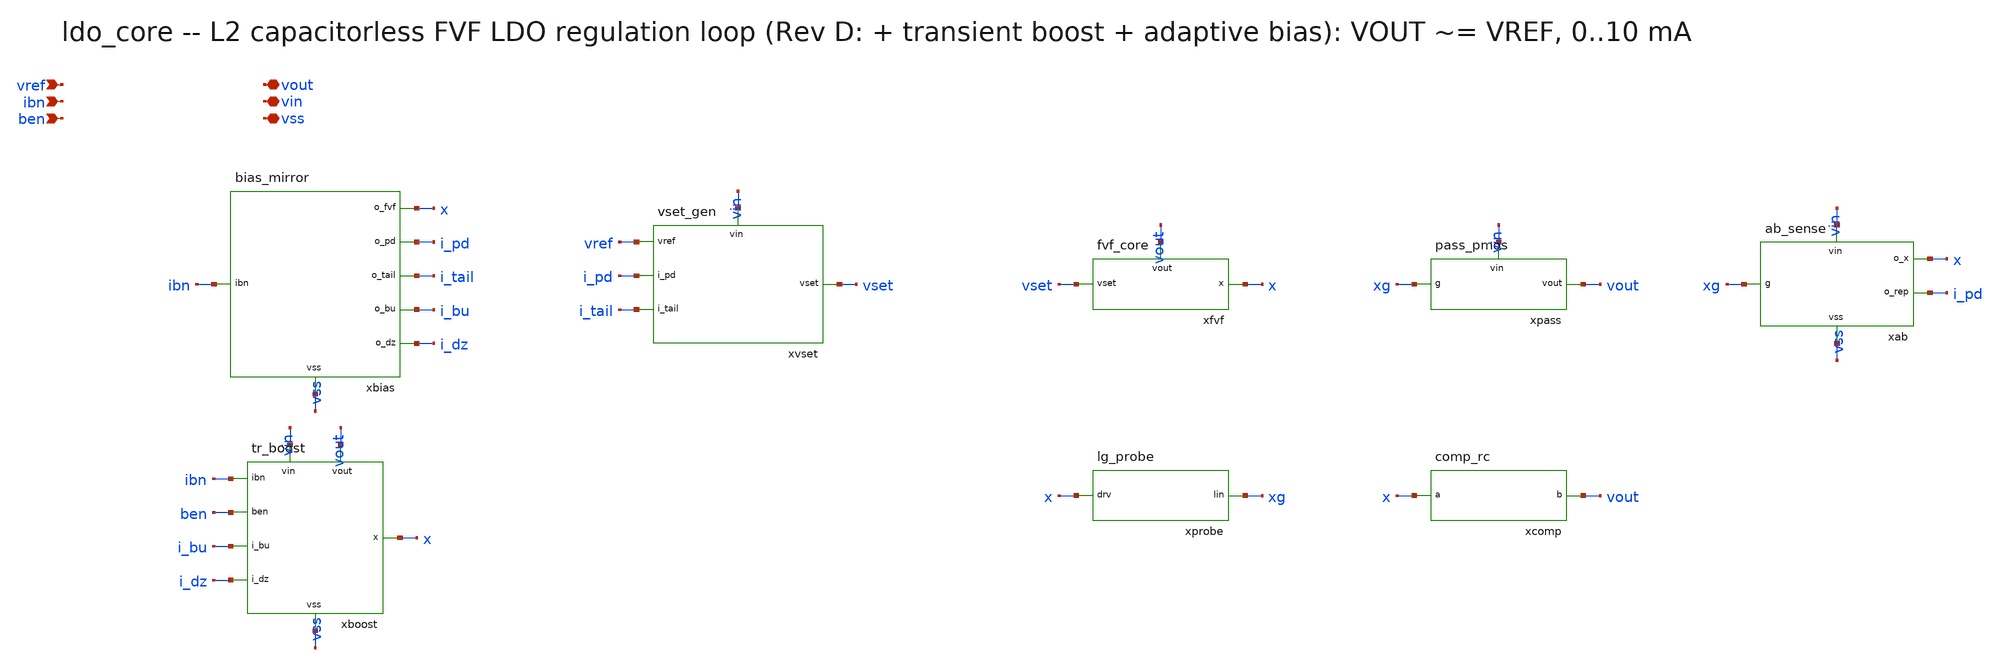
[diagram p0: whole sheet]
** sch_path: xschem/onetops/ldo_core.sch
**.subckt ldo_core vref ibn ben vout vin vss
*.ipin vref
*.ipin ibn
*.ipin ben
*.iopin vout
*.iopin vin
*.iopin vss
xbias ibn x i_pd i_tail i_bu i_dz vss bias_mirror
xboost ibn ben i_bu i_dz x vin vout vss tr_boost
xvset vref i_pd i_tail vset vin vset_gen
xfvf vset x vout fvf_core
xprobe x xg lg_probe
xpass xg vout vin pass_pmos
xcomp x vout comp_rc
xab xg x i_pd vin vss ab_sense
**.ends

* expanding   symbol:  onetops/bias_mirror.sym # of pins=7
** sym_path: xschem/onetops/bias_mirror.sym
** sch_path: xschem/onetops/bias_mirror.sch
.subckt bias_mirror ibn o_fvf o_pd o_tail o_bu o_dz vss
*.ipin ibn
*.opin o_fvf
*.opin o_pd
*.opin o_tail
*.opin o_bu
*.opin o_dz
*.iopin vss
XMN0 ibn ibn vss vss sky130_fd_pr__nfet_01v8 L=1 W=4 nf=1 ad='int((1 + 1)/2) * 4 / 1 * 0.29' as='int((1 + 2)/2) * 4 / 1 * 0.29'
+ pd='2*int((1 + 1)/2) * (4 / 1 + 0.29)' ps='2*int((1 + 2)/2) * (4 / 1 + 0.29)' nrd='0.29 / 4 ' nrs='0.29 / 4 '
+ sa=0 sb=0 sd=0 mult=1 m=1
XMN1 o_fvf ibn vss vss sky130_fd_pr__nfet_01v8 L=1 W=1 nf=1 ad='int((1 + 1)/2) * 1 / 1 * 0.29' as='int((1 + 2)/2) * 1 / 1 * 0.29'
+ pd='2*int((1 + 1)/2) * (1 / 1 + 0.29)' ps='2*int((1 + 2)/2) * (1 / 1 + 0.29)' nrd='0.29 / 1 ' nrs='0.29 / 1 '
+ sa=0 sb=0 sd=0 mult=1 m=1
XMN2 o_bu ibn vss vss sky130_fd_pr__nfet_01v8 L=1 W=4 nf=1 ad='int((1 + 1)/2) * 4 / 1 * 0.29' as='int((1 + 2)/2) * 4 / 1 * 0.29'
+ pd='2*int((1 + 1)/2) * (4 / 1 + 0.29)' ps='2*int((1 + 2)/2) * (4 / 1 + 0.29)' nrd='0.29 / 4 ' nrs='0.29 / 4 '
+ sa=0 sb=0 sd=0 mult=1 m=1
XMN3 o_pd ibn vss vss sky130_fd_pr__nfet_01v8 L=1 W=1 nf=1 ad='int((1 + 1)/2) * 1 / 1 * 0.29' as='int((1 + 2)/2) * 1 / 1 * 0.29'
+ pd='2*int((1 + 1)/2) * (1 / 1 + 0.29)' ps='2*int((1 + 2)/2) * (1 / 1 + 0.29)' nrd='0.29 / 1 ' nrs='0.29 / 1 '
+ sa=0 sb=0 sd=0 mult=1 m=1
XMN4 o_tail ibn vss vss sky130_fd_pr__nfet_01v8 L=1 W=4 nf=1 ad='int((1 + 1)/2) * 4 / 1 * 0.29' as='int((1 + 2)/2) * 4 / 1 * 0.29'
+ pd='2*int((1 + 1)/2) * (4 / 1 + 0.29)' ps='2*int((1 + 2)/2) * (4 / 1 + 0.29)' nrd='0.29 / 4 ' nrs='0.29 / 4 '
+ sa=0 sb=0 sd=0 mult=2 m=2
XMN5 o_dz ibn vss vss sky130_fd_pr__nfet_01v8 L=1 W=4 nf=1 ad='int((1 + 1)/2) * 4 / 1 * 0.29' as='int((1 + 2)/2) * 4 / 1 * 0.29'
+ pd='2*int((1 + 1)/2) * (4 / 1 + 0.29)' ps='2*int((1 + 2)/2) * (4 / 1 + 0.29)' nrd='0.29 / 4 ' nrs='0.29 / 4 '
+ sa=0 sb=0 sd=0 mult=1 m=1
.ends


* expanding   symbol:  onetops/tr_boost.sym # of pins=8
** sym_path: xschem/onetops/tr_boost.sym
** sch_path: xschem/onetops/tr_boost.sch
.subckt tr_boost ibn ben i_bu i_dz x vin vout vss
*.ipin ibn
*.ipin ben
*.iopin i_bu
*.iopin i_dz
*.iopin x
*.iopin vin
*.iopin vout
*.iopin vss
XMPB0 i_bu i_bu vin vin sky130_fd_pr__pfet_01v8_lvt L=0.5 W=40 nf=1 ad='int((1 + 1)/2) * 40 / 1 * 0.29'
+ as='int((1 + 2)/2) * 40 / 1 * 0.29' pd='2*int((1 + 1)/2) * (40 / 1 + 0.29)' ps='2*int((1 + 2)/2) * (40 / 1 + 0.29)'
+ nrd='0.29 / 40 ' nrs='0.29 / 40 ' sa=0 sb=0 sd=0 mult=1 m=1
Rbu i_bu gsu 1Meg m=1
Cbu vout gsu 0.5p m=1
XMPB1 i_dz gsu vin vin sky130_fd_pr__pfet_01v8_lvt L=0.5 W=20 nf=1 ad='int((1 + 1)/2) * 20 / 1 * 0.29'
+ as='int((1 + 2)/2) * 20 / 1 * 0.29' pd='2*int((1 + 1)/2) * (20 / 1 + 0.29)' ps='2*int((1 + 2)/2) * (20 / 1 + 0.29)'
+ nrd='0.29 / 20 ' nrs='0.29 / 20 ' sa=0 sb=0 sd=0 mult=1 m=1
XMNB0 i_dz i_dz vss vss sky130_fd_pr__nfet_01v8 L=0.5 W=2 nf=1 ad='int((1 + 1)/2) * 2 / 1 * 0.29' as='int((1 + 2)/2) * 2 / 1 * 0.29'
+ pd='2*int((1 + 1)/2) * (2 / 1 + 0.29)' ps='2*int((1 + 2)/2) * (2 / 1 + 0.29)' nrd='0.29 / 2 ' nrs='0.29 / 2 '
+ sa=0 sb=0 sd=0 mult=1 m=1
XMNB1 nsw i_dz vss vss sky130_fd_pr__nfet_01v8 L=0.5 W=2 nf=1 ad='int((1 + 1)/2) * 2 / 1 * 0.29' as='int((1 + 2)/2) * 2 / 1 * 0.29'
+ pd='2*int((1 + 1)/2) * (2 / 1 + 0.29)' ps='2*int((1 + 2)/2) * (2 / 1 + 0.29)' nrd='0.29 / 2 ' nrs='0.29 / 2 '
+ sa=0 sb=0 sd=0 mult=20 m=20
XMSW x ben nsw vss sky130_fd_pr__nfet_01v8 L=0.15 W=10 nf=1 ad='int((1 + 1)/2) * 10 / 1 * 0.29' as='int((1 + 2)/2) * 10 / 1 * 0.29'
+ pd='2*int((1 + 1)/2) * (10 / 1 + 0.29)' ps='2*int((1 + 2)/2) * (10 / 1 + 0.29)' nrd='0.29 / 10 ' nrs='0.29 / 10 '
+ sa=0 sb=0 sd=0 mult=1 m=1
Rbo ibn gso 1Meg m=1
Cbo vout gso 0.5p m=1
XMND vout gso vss vss sky130_fd_pr__nfet_01v8 L=1 W=4 nf=1 ad='int((1 + 1)/2) * 4 / 1 * 0.29' as='int((1 + 2)/2) * 4 / 1 * 0.29'
+ pd='2*int((1 + 1)/2) * (4 / 1 + 0.29)' ps='2*int((1 + 2)/2) * (4 / 1 + 0.29)' nrd='0.29 / 4 ' nrs='0.29 / 4 '
+ sa=0 sb=0 sd=0 mult=2 m=2
XMPDZ ndo i_bu vin vin sky130_fd_pr__pfet_01v8_lvt L=0.5 W=40 nf=1 ad='int((1 + 1)/2) * 40 / 1 * 0.29'
+ as='int((1 + 2)/2) * 40 / 1 * 0.29' pd='2*int((1 + 1)/2) * (40 / 1 + 0.29)' ps='2*int((1 + 2)/2) * (40 / 1 + 0.29)'
+ nrd='0.29 / 40 ' nrs='0.29 / 40 ' sa=0 sb=0 sd=0 mult=1 m=1
XMNS1 ndo gso vss vss sky130_fd_pr__nfet_01v8 L=1 W=2 nf=1 ad='int((1 + 1)/2) * 2 / 1 * 0.29' as='int((1 + 2)/2) * 2 / 1 * 0.29'
+ pd='2*int((1 + 1)/2) * (2 / 1 + 0.29)' ps='2*int((1 + 2)/2) * (2 / 1 + 0.29)' nrd='0.29 / 2 ' nrs='0.29 / 2 '
+ sa=0 sb=0 sd=0 mult=1 m=1
XMPO0 ndo ndo vin vin sky130_fd_pr__pfet_01v8 L=0.5 W=4 nf=1 ad='int((1 + 1)/2) * 4 / 1 * 0.29' as='int((1 + 2)/2) * 4 / 1 * 0.29'
+ pd='2*int((1 + 1)/2) * (4 / 1 + 0.29)' ps='2*int((1 + 2)/2) * (4 / 1 + 0.29)' nrd='0.29 / 4 ' nrs='0.29 / 4 '
+ sa=0 sb=0 sd=0 mult=1 m=1
XMPO1 psw ndo vin vin sky130_fd_pr__pfet_01v8 L=0.5 W=4 nf=1 ad='int((1 + 1)/2) * 4 / 1 * 0.29' as='int((1 + 2)/2) * 4 / 1 * 0.29'
+ pd='2*int((1 + 1)/2) * (4 / 1 + 0.29)' ps='2*int((1 + 2)/2) * (4 / 1 + 0.29)' nrd='0.29 / 4 ' nrs='0.29 / 4 '
+ sa=0 sb=0 sd=0 mult=20 m=20
XMPSW x benb psw vin sky130_fd_pr__pfet_01v8 L=0.15 W=20 nf=1 ad='int((1 + 1)/2) * 20 / 1 * 0.29' as='int((1 + 2)/2) * 20 / 1 * 0.29'
+ pd='2*int((1 + 1)/2) * (20 / 1 + 0.29)' ps='2*int((1 + 2)/2) * (20 / 1 + 0.29)' nrd='0.29 / 20 ' nrs='0.29 / 20 '
+ sa=0 sb=0 sd=0 mult=1 m=1
xinv ben benb vin vss inv
.ends


* expanding   symbol:  onetops/vset_gen.sym # of pins=5
** sym_path: xschem/onetops/vset_gen.sym
** sch_path: xschem/onetops/vset_gen.sch
.subckt vset_gen vref i_pd i_tail vset vin
*.ipin vref
*.opin vset
*.iopin i_pd
*.iopin i_tail
*.iopin vin
XMPD i_pd i_pd vin vin sky130_fd_pr__pfet_01v8_lvt L=2 W=10 nf=1 ad='int((1 + 1)/2) * 10 / 1 * 0.29'
+ as='int((1 + 2)/2) * 10 / 1 * 0.29' pd='2*int((1 + 1)/2) * (10 / 1 + 0.29)' ps='2*int((1 + 2)/2) * (10 / 1 + 0.29)'
+ nrd='0.29 / 10 ' nrs='0.29 / 10 ' sa=0 sb=0 sd=0 mult=1 m=1
XMPS vrep i_pd vin vin sky130_fd_pr__pfet_01v8_lvt L=2 W=10 nf=1 ad='int((1 + 1)/2) * 10 / 1 * 0.29'
+ as='int((1 + 2)/2) * 10 / 1 * 0.29' pd='2*int((1 + 1)/2) * (10 / 1 + 0.29)' ps='2*int((1 + 2)/2) * (10 / 1 + 0.29)'
+ nrd='0.29 / 10 ' nrs='0.29 / 10 ' sa=0 sb=0 sd=0 mult=1 m=1
XMR 0 vset vrep vrep sky130_fd_pr__pfet_01v8_lvt L=1 W=100 nf=1 ad='int((1 + 1)/2) * 100 / 1 * 0.29'
+ as='int((1 + 2)/2) * 100 / 1 * 0.29' pd='2*int((1 + 1)/2) * (100 / 1 + 0.29)' ps='2*int((1 + 2)/2) * (100 / 1 + 0.29)'
+ nrd='0.29 / 100 ' nrs='0.29 / 100 ' sa=0 sb=0 sd=0 mult=1 m=1
xota vref vrep i_tail vset vin ota5t
Cset vset 0 2p m=1
.ends


* expanding   symbol:  onetops/fvf_core.sym # of pins=3
** sym_path: xschem/onetops/fvf_core.sym
** sch_path: xschem/onetops/fvf_core.sch
.subckt fvf_core vset x vout
*.ipin vset
*.opin x
*.iopin vout
XMC x vset vout vout sky130_fd_pr__pfet_01v8_lvt L=1 W=100 nf=1 ad='int((1 + 1)/2) * 100 / 1 * 0.29'
+ as='int((1 + 2)/2) * 100 / 1 * 0.29' pd='2*int((1 + 1)/2) * (100 / 1 + 0.29)' ps='2*int((1 + 2)/2) * (100 / 1 + 0.29)'
+ nrd='0.29 / 100 ' nrs='0.29 / 100 ' sa=0 sb=0 sd=0 mult=1 m=1
.ends


* expanding   symbol:  onetops/lg_probe.sym # of pins=2
** sym_path: xschem/onetops/lg_probe.sym
** sch_path: xschem/onetops/lg_probe.sch
.subckt lg_probe drv lin
*.iopin drv
*.iopin lin
Vbrk lin drv dc 0 ac 0
Iinj 0 lin dc 0 ac 0
.ends


* expanding   symbol:  onetops/pass_pmos.sym # of pins=3
** sym_path: xschem/onetops/pass_pmos.sym
** sch_path: xschem/onetops/pass_pmos.sch
.subckt pass_pmos g vout vin
*.ipin g
*.iopin vin
*.iopin vout
XMP vout g vin vin sky130_fd_pr__pfet_01v8 L=0.35 W=10 nf=1 ad='int((1 + 1)/2) * 10 / 1 * 0.29' as='int((1 + 2)/2) * 10 / 1 * 0.29'
+ pd='2*int((1 + 1)/2) * (10 / 1 + 0.29)' ps='2*int((1 + 2)/2) * (10 / 1 + 0.29)' nrd='0.29 / 10 ' nrs='0.29 / 10 '
+ sa=0 sb=0 sd=0 mult=70 m=70
.ends


* expanding   symbol:  onetops/comp_rc.sym # of pins=2
** sym_path: xschem/onetops/comp_rc.sym
** sch_path: xschem/onetops/comp_rc.sch
.subckt comp_rc a b
*.iopin a
*.iopin b
Rz a n1 1 m=1
Cc n1 b 4p m=1
.ends


* expanding   symbol:  onetops/ab_sense.sym # of pins=5
** sym_path: xschem/onetops/ab_sense.sym
** sch_path: xschem/onetops/ab_sense.sch
.subckt ab_sense g o_x o_rep vin vss
*.ipin g
*.opin o_x
*.opin o_rep
*.iopin vin
*.iopin vss
XMS ns g vin vin sky130_fd_pr__pfet_01v8 L=0.35 W=1.4 nf=1 ad='int((1 + 1)/2) * 1.4 / 1 * 0.29' as='int((1 + 2)/2) * 1.4 / 1 * 0.29'
+ pd='2*int((1 + 1)/2) * (1.4 / 1 + 0.29)' ps='2*int((1 + 2)/2) * (1.4 / 1 + 0.29)' nrd='0.29 / 1.4 ' nrs='0.29 / 1.4 '
+ sa=0 sb=0 sd=0 mult=1 m=1
XMSD ns ns vss vss sky130_fd_pr__nfet_01v8 L=1 W=4 nf=1 ad='int((1 + 1)/2) * 4 / 1 * 0.29' as='int((1 + 2)/2) * 4 / 1 * 0.29'
+ pd='2*int((1 + 1)/2) * (4 / 1 + 0.29)' ps='2*int((1 + 2)/2) * (4 / 1 + 0.29)' nrd='0.29 / 4 ' nrs='0.29 / 4 '
+ sa=0 sb=0 sd=0 mult=1 m=1
XMSX o_x ns vss vss sky130_fd_pr__nfet_01v8 L=1 W=4 nf=1 ad='int((1 + 1)/2) * 4 / 1 * 0.29' as='int((1 + 2)/2) * 4 / 1 * 0.29'
+ pd='2*int((1 + 1)/2) * (4 / 1 + 0.29)' ps='2*int((1 + 2)/2) * (4 / 1 + 0.29)' nrd='0.29 / 4 ' nrs='0.29 / 4 '
+ sa=0 sb=0 sd=0 mult=1 m=1
XMSR o_rep ns vss vss sky130_fd_pr__nfet_01v8 L=1 W=4 nf=1 ad='int((1 + 1)/2) * 4 / 1 * 0.29' as='int((1 + 2)/2) * 4 / 1 * 0.29'
+ pd='2*int((1 + 1)/2) * (4 / 1 + 0.29)' ps='2*int((1 + 2)/2) * (4 / 1 + 0.29)' nrd='0.29 / 4 ' nrs='0.29 / 4 '
+ sa=0 sb=0 sd=0 mult=1 m=1
.ends


* expanding   symbol:  onetops/inv.sym # of pins=4
** sym_path: xschem/onetops/inv.sym
** sch_path: xschem/onetops/inv.sch
.subckt inv a y vdd vss
*.ipin a
*.opin y
*.iopin vdd
*.iopin vss
XMP1 y a vdd vdd sky130_fd_pr__pfet_01v8 L=0.15 W=2 nf=1 ad='int((1 + 1)/2) * 2 / 1 * 0.29' as='int((1 + 2)/2) * 2 / 1 * 0.29'
+ pd='2*int((1 + 1)/2) * (2 / 1 + 0.29)' ps='2*int((1 + 2)/2) * (2 / 1 + 0.29)' nrd='0.29 / 2 ' nrs='0.29 / 2 '
+ sa=0 sb=0 sd=0 mult=1 m=1
XMN1 y a vss vss sky130_fd_pr__nfet_01v8 L=0.15 W=1 nf=1 ad='int((1 + 1)/2) * 1 / 1 * 0.29' as='int((1 + 2)/2) * 1 / 1 * 0.29'
+ pd='2*int((1 + 1)/2) * (1 / 1 + 0.29)' ps='2*int((1 + 2)/2) * (1 / 1 + 0.29)' nrd='0.29 / 1 ' nrs='0.29 / 1 '
+ sa=0 sb=0 sd=0 mult=1 m=1
.ends


* expanding   symbol:  onetops/ota5t.sym # of pins=5
** sym_path: xschem/onetops/ota5t.sym
** sch_path: xschem/onetops/ota5t.sch
.subckt ota5t inp inn tail out vdd
*.ipin inp
*.ipin inn
*.opin out
*.iopin tail
*.iopin vdd
XMP1 nd nd vdd vdd sky130_fd_pr__pfet_01v8_lvt L=2 W=20 nf=1 ad='int((1 + 1)/2) * 20 / 1 * 0.29' as='int((1 + 2)/2) * 20 / 1 * 0.29'
+ pd='2*int((1 + 1)/2) * (20 / 1 + 0.29)' ps='2*int((1 + 2)/2) * (20 / 1 + 0.29)' nrd='0.29 / 20 ' nrs='0.29 / 20 '
+ sa=0 sb=0 sd=0 mult=1 m=1
XMP2 out nd vdd vdd sky130_fd_pr__pfet_01v8_lvt L=2 W=20 nf=1 ad='int((1 + 1)/2) * 20 / 1 * 0.29' as='int((1 + 2)/2) * 20 / 1 * 0.29'
+ pd='2*int((1 + 1)/2) * (20 / 1 + 0.29)' ps='2*int((1 + 2)/2) * (20 / 1 + 0.29)' nrd='0.29 / 20 ' nrs='0.29 / 20 '
+ sa=0 sb=0 sd=0 mult=1 m=1
XMN1 nd inp tail 0 sky130_fd_pr__nfet_01v8 L=1 W=5 nf=1 ad='int((1 + 1)/2) * 5 / 1 * 0.29' as='int((1 + 2)/2) * 5 / 1 * 0.29'
+ pd='2*int((1 + 1)/2) * (5 / 1 + 0.29)' ps='2*int((1 + 2)/2) * (5 / 1 + 0.29)' nrd='0.29 / 5 ' nrs='0.29 / 5 '
+ sa=0 sb=0 sd=0 mult=1 m=1
XMN2 out inn tail 0 sky130_fd_pr__nfet_01v8 L=1 W=5 nf=1 ad='int((1 + 1)/2) * 5 / 1 * 0.29' as='int((1 + 2)/2) * 5 / 1 * 0.29'
+ pd='2*int((1 + 1)/2) * (5 / 1 + 0.29)' ps='2*int((1 + 2)/2) * (5 / 1 + 0.29)' nrd='0.29 / 5 ' nrs='0.29 / 5 '
+ sa=0 sb=0 sd=0 mult=1 m=1
.ends

.end
